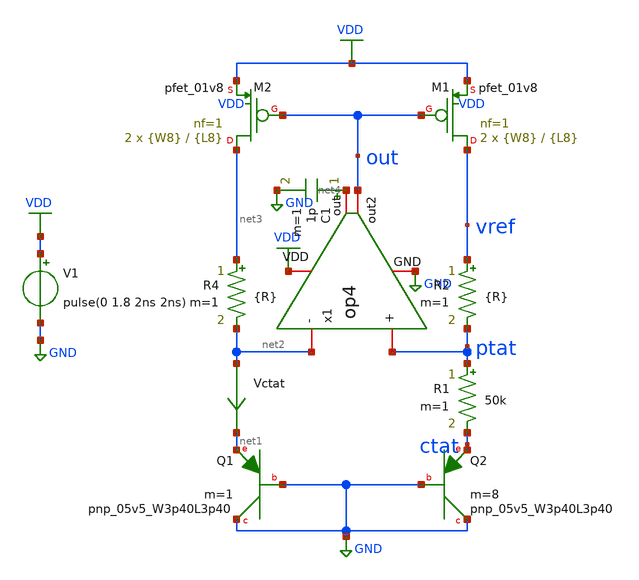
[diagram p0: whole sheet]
** sch_path: xschem/bgr_op4.sch
**.subckt bgr_op4
XQ1 GND GND net1 sky130_fd_pr__pnp_05v5_W3p40L3p40 m=1
XQ2 GND GND ctat sky130_fd_pr__pnp_05v5_W3p40L3p40 m=8
Vctat net2 net1 0
.save i(vctat)
V1 VDD GND pulse(0 1.8 2ns 2ns)
XM1 vref out VDD VDD sky130_fd_pr__pfet_01v8 L={L8} W={W8} nf=1 ad='int((nf+1)/2) * W/nf * 0.29' as='int((nf+2)/2) * W/nf * 0.29'
+ pd='2*int((nf+1)/2) * (W/nf + 0.29)' ps='2*int((nf+2)/2) * (W/nf + 0.29)' nrd='0.29 / W' nrs='0.29 / W'
+ sa=0 sb=0 sd=0 mult=2 m=2
XM2 net3 out VDD VDD sky130_fd_pr__pfet_01v8 L={L8} W={W8} nf=1 ad='int((nf+1)/2) * W/nf * 0.29' as='int((nf+2)/2) * W/nf * 0.29'
+ pd='2*int((nf+1)/2) * (W/nf + 0.29)' ps='2*int((nf+2)/2) * (W/nf + 0.29)' nrd='0.29 / W' nrs='0.29 / W'
+ sa=0 sb=0 sd=0 mult=2 m=2
R1 ptat ctat 50k m=1
R2 vref ptat {R} m=1
R4 net3 net2 {R} m=1
x1 VDD net4 out net2 ptat GND op4
C1 net4 GND 1p m=1
**** begin user architecture code


.param L8=5
.param W8=1
.param R=486k



** opencircuitdesign pdks install
.lib $::SKYWATER_MODELS/sky130.lib.spice tt




.option savecurrents
.control
save all
op
remzerovec
write bgr_op4.raw
set appendwrite

dc temp -40 85 1
remzerovec
write bgr_op4.raw
*plot (ptat-ctat)
*plot ctat
plot vref

********TC********
meas dc temp_avg_vref avg v(vref)
meas dc temp_vref_27 find v(vref) when temp-sweep=27
meas dc temp_pp_vref PP v(vref)
meas dc temp_vref_max max v(vref)
meas dc temp_max_vref when v(vref)='temp_vref_max'
meas dc temp_vref_min min v(vref)
meas dc temp_min_vref when v(vref)='temp_vref_min'
let vref_tc='((temp_pp_vref*1000000)/(125*temp_avg_vref))'
print vref_tc

******PSRR******
ac dec 1000 1 10Meg
write bgr_op4.raw
remzerovec
plot vdb(vref)
meas ac psrr_100 find vdb(vref) at=100
meas ac psrr_1k find vdb(vref) at=1k

****Power****
tran 10us 100ms
write bgr_op4.raw
remzerovec
meas tran ave_v avg vdd
meas tran ave_i avg i(v1)
let ave_power='ave_v*(-ave_i)
plot vdd vref
*plot -i(v1)
print ave_power

*******LS******
dc v1 0 3.5 0.1
write bgr_op4.raw
remzerovec
plot vdd vref
meas dc vref_min min v(vref) from=1.62 to=1.98
meas dc vref_pp PP v(vref) from=1.62 to=1.98
let line_reg='100*(vref_pp)/(vref_min*(1.98-1.62))'
print line_reg

.endc


**** end user architecture code
**.ends

* expanding   symbol:  op4.sym # of pins=6
** sym_path: xschem/op4.sym
** sch_path: xschem/op4.sch
.subckt op4 VDD out out2 - + GND
*.iopin VDD
*.iopin GND
*.iopin -
*.iopin +
*.iopin out
*.iopin out2
C2 out2 net4 1p m=1
R2 net4 out 1k m=1
XM1 bias bias net5 GND sky130_fd_pr__nfet_01v8 L={L5} W={W5} nf=1 ad='int((nf+1)/2) * W/nf * 0.29' as='int((nf+2)/2)
+ * W/nf * 0.29' pd='2*int((nf+1)/2) * (W/nf + 0.29)' ps='2*int((nf+2)/2) * (W/nf + 0.29)' nrd='0.29 /
+ W' nrs='0.29 / W' sa=0 sb=0 sd=0 mult=2 m=2
XM2 net3 bias GND GND sky130_fd_pr__nfet_01v8 L={L5} W={W5} nf=1 ad='int((nf+1)/2) * W/nf * 0.29' as='int((nf+2)/2)
+ * W/nf * 0.29' pd='2*int((nf+1)/2) * (W/nf + 0.29)' ps='2*int((nf+2)/2) * (W/nf + 0.29)' nrd='0.29 /
+ W' nrs='0.29 / W' sa=0 sb=0 sd=0 mult=2 m=2
XM3 net1 - net2 GND sky130_fd_pr__nfet_01v8 L={L4} W={W4} nf=1 ad='int((nf+1)/2) * W/nf * 0.29' as='int((nf+2)/2)
+ * W/nf * 0.29' pd='2*int((nf+1)/2) * (W/nf + 0.29)' ps='2*int((nf+2)/2) * (W/nf + 0.29)' nrd='0.29 /
+ W' nrs='0.29 / W' sa=0 sb=0 sd=0 mult=2 m=2
XM4 out + net2 GND sky130_fd_pr__nfet_01v8 L={L4} W={W4} nf=1 ad='int((nf+1)/2) * W/nf * 0.29' as='int((nf+2)/2)
+ * W/nf * 0.29' pd='2*int((nf+1)/2) * (W/nf + 0.29)' ps='2*int((nf+2)/2) * (W/nf + 0.29)' nrd='0.29 /
+ W' nrs='0.29 / W' sa=0 sb=0 sd=0 mult=2 m=2
XM6 bias net3 VDD VDD sky130_fd_pr__pfet_01v8 L={L1} W={W1} nf=1 ad='int((nf+1)/2) * W/nf * 0.29' as='int((nf+2)/2)
+ * W/nf * 0.29' pd='2*int((nf+1)/2) * (W/nf + 0.29)' ps='2*int((nf+2)/2) * (W/nf + 0.29)' nrd='0.29 /
+ W' nrs='0.29 / W' sa=0 sb=0 sd=0 mult=2 m=2
XM7 net3 net3 VDD VDD sky130_fd_pr__pfet_01v8 L={L1} W={W1} nf=1 ad='int((nf+1)/2) * W/nf * 0.29' as='int((nf+2)/2)
+ * W/nf * 0.29' pd='2*int((nf+1)/2) * (W/nf + 0.29)' ps='2*int((nf+2)/2) * (W/nf + 0.29)' nrd='0.29 /
+ W' nrs='0.29 / W' sa=0 sb=0 sd=0 mult=2 m=2
XM8 out net1 VDD VDD sky130_fd_pr__pfet_01v8 L={L7} W={W7} nf=1 ad='int((nf+1)/2) * W/nf * 0.29' as='int((nf+2)/2)
+ * W/nf * 0.29' pd='2*int((nf+1)/2) * (W/nf + 0.29)' ps='2*int((nf+2)/2) * (W/nf + 0.29)' nrd='0.29 /
+ W' nrs='0.29 / W' sa=0 sb=0 sd=0 mult=4 m=4
XM9 net1 net1 VDD VDD sky130_fd_pr__pfet_01v8 L={L7} W={W7} nf=1 ad='int((nf+1)/2) * W/nf * 0.29' as='int((nf+2)/2)
+ * W/nf * 0.29' pd='2*int((nf+1)/2) * (W/nf + 0.29)' ps='2*int((nf+2)/2) * (W/nf + 0.29)' nrd='0.29 /
+ W' nrs='0.29 / W' sa=0 sb=0 sd=0 mult=4 m=4
XM5 net2 bias GND GND sky130_fd_pr__nfet_01v8 L={L6} W={W6} nf=1 ad='int((nf+1)/2) * W/nf * 0.29' as='int((nf+2)/2)
+ * W/nf * 0.29' pd='2*int((nf+1)/2) * (W/nf + 0.29)' ps='2*int((nf+2)/2) * (W/nf + 0.29)' nrd='0.29 /
+ W' nrs='0.29 / W' sa=0 sb=0 sd=0 mult=2 m=2
XM10 out2 out VDD VDD sky130_fd_pr__pfet_01v8 L={L2} W={W2} nf=1 ad='int((nf+1)/2) * W/nf * 0.29' as='int((nf+2)/2)
+ * W/nf * 0.29' pd='2*int((nf+1)/2) * (W/nf + 0.29)' ps='2*int((nf+2)/2) * (W/nf + 0.29)' nrd='0.29 /
+ W' nrs='0.29 / W' sa=0 sb=0 sd=0 mult=4 m=4
XM11 out2 bias GND GND sky130_fd_pr__nfet_01v8 L={L3} W={W3} nf=1 ad='int((nf+1)/2) * W/nf * 0.29' as='int((nf+2)/2)
+ * W/nf * 0.29' pd='2*int((nf+1)/2) * (W/nf + 0.29)' ps='2*int((nf+2)/2) * (W/nf + 0.29)' nrd='0.29 /
+ W' nrs='0.29 / W' sa=0 sb=0 sd=0 mult=2 m=2
R3 net5 GND 4.5k m=1
**** begin user architecture code


**************
*PMOS cms
.param L1=40
.param W1=1

**************
*NMOS cms
.param L5=20
.param W5=1

**************
*PMOS differential
.param L7=10
.param W7=0.5

**************
*differential Pair
.param L4=10
.param W4=1.5

**************
*NMOS current control
.param L6=5
.param W6=1

**************
*Second Stage
.param L2=30
.param W2=1

**************
*NMOS current second stage
.param L3=20
.param W3=0.5


**** end user architecture code
.ends

.GLOBAL VDD
.GLOBAL GND
.end
